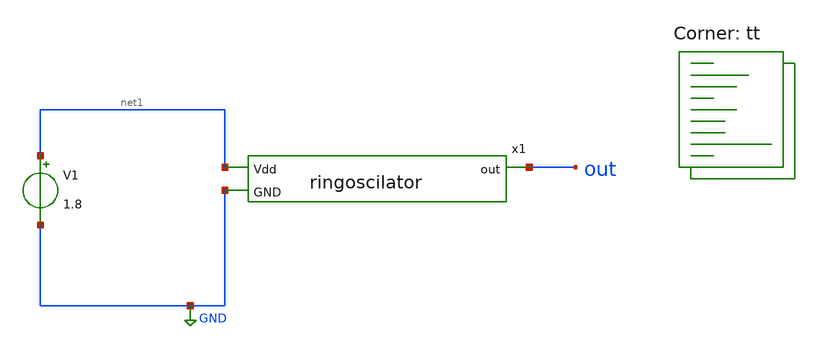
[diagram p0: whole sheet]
** sch_path: RING OSCILLATOR/tb_ringoscilator.sch
**.subckt tb_ringoscilator
V1 net1 GND 1.8
x1 net1 out GND ringoscilator
**** begin user architecture code
.lib $::SKYWATER_MODELS/sky130.lib.spice tt


.option wnflag=0
.option savecurrents
.control
save all
tran 1ps 4ns
plot out
op
.endc


**** end user architecture code
**.ends
.GLOBAL GND
.end
